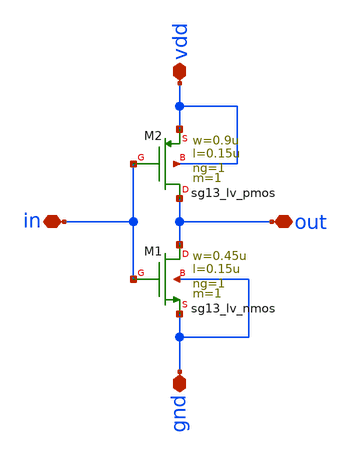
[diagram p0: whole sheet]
** sch_path: inversor.sch
**.subckt inversor out vdd gnd in
*.iopin out
*.iopin vdd
*.iopin gnd
*.iopin in
XM1 out in gnd gnd sg13_lv_nmos w=0.45u l=0.15u ng=1 m=1 mm_ok=1
XM2 out in vdd vdd sg13_lv_pmos w=0.9u l=0.15u ng=1 m=1 mm_ok=1
**.ends
.end
